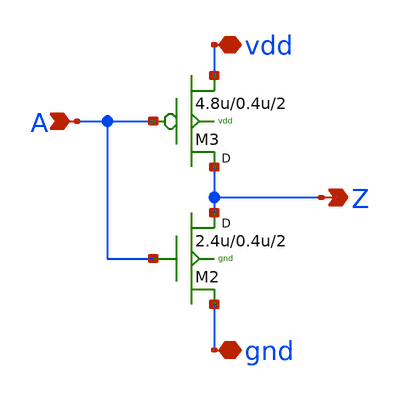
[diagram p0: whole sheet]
** sch_path: sram_2_64_scn4m_lcc/pinv_14.sch
**.subckt pinv_14 A Z vdd gnd
*.ipin A
*.opin Z
*.iopin vdd
*.iopin gnd
M2 Z A gnd gnd n w=2.4u l=0.4u m=2
M3 Z A vdd vdd p w=4.8u l=0.4u m=2
**.ends
.end
